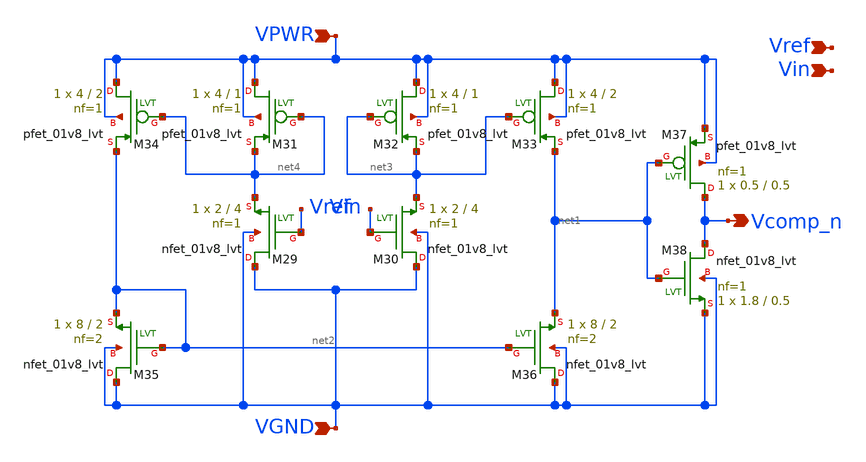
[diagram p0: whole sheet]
** sch_path: xschem/subckts/NComp.sch
**.subckt NComp Vcomp_n Vin Vref VPWR VGND
*.opin Vcomp_n
*.ipin Vin
*.ipin Vref
*.ipin VPWR
*.ipin VGND
XM29 VGND Vref net4 VGND sky130_fd_pr__nfet_01v8_lvt L=4 W=2 nf=1 ad='int((nf+1)/2) * W/nf * 0.29' as='int((nf+2)/2) * W/nf * 0.29'
+ pd='2*int((nf+1)/2) * (W/nf + 0.29)' ps='2*int((nf+2)/2) * (W/nf + 0.29)' nrd='0.29 / W' nrs='0.29 / W'
+ sa=0 sb=0 sd=0 mult=1 m=1
XM30 VGND Vin net3 VGND sky130_fd_pr__nfet_01v8_lvt L=4 W=2 nf=1 ad='int((nf+1)/2) * W/nf * 0.29' as='int((nf+2)/2) * W/nf * 0.29'
+ pd='2*int((nf+1)/2) * (W/nf + 0.29)' ps='2*int((nf+2)/2) * (W/nf + 0.29)' nrd='0.29 / W' nrs='0.29 / W'
+ sa=0 sb=0 sd=0 mult=1 m=1
XM31 VPWR net4 net4 VPWR sky130_fd_pr__pfet_01v8_lvt L=1 W=4 nf=1 ad='int((nf+1)/2) * W/nf * 0.29' as='int((nf+2)/2) * W/nf * 0.29'
+ pd='2*int((nf+1)/2) * (W/nf + 0.29)' ps='2*int((nf+2)/2) * (W/nf + 0.29)' nrd='0.29 / W' nrs='0.29 / W'
+ sa=0 sb=0 sd=0 mult=1 m=1
XM32 VPWR net3 net3 VPWR sky130_fd_pr__pfet_01v8_lvt L=1 W=4 nf=1 ad='int((nf+1)/2) * W/nf * 0.29' as='int((nf+2)/2) * W/nf * 0.29'
+ pd='2*int((nf+1)/2) * (W/nf + 0.29)' ps='2*int((nf+2)/2) * (W/nf + 0.29)' nrd='0.29 / W' nrs='0.29 / W'
+ sa=0 sb=0 sd=0 mult=1 m=1
XM33 VPWR net3 net1 VPWR sky130_fd_pr__pfet_01v8_lvt L=2 W=4 nf=1 ad='int((nf+1)/2) * W/nf * 0.29' as='int((nf+2)/2) * W/nf * 0.29'
+ pd='2*int((nf+1)/2) * (W/nf + 0.29)' ps='2*int((nf+2)/2) * (W/nf + 0.29)' nrd='0.29 / W' nrs='0.29 / W'
+ sa=0 sb=0 sd=0 mult=1 m=1
XM34 VPWR net4 net2 VPWR sky130_fd_pr__pfet_01v8_lvt L=2 W=4 nf=1 ad='int((nf+1)/2) * W/nf * 0.29' as='int((nf+2)/2) * W/nf * 0.29'
+ pd='2*int((nf+1)/2) * (W/nf + 0.29)' ps='2*int((nf+2)/2) * (W/nf + 0.29)' nrd='0.29 / W' nrs='0.29 / W'
+ sa=0 sb=0 sd=0 mult=1 m=1
XM35 VGND net2 net2 VGND sky130_fd_pr__nfet_01v8_lvt L=2 W=8 nf=2 ad='int((nf+1)/2) * W/nf * 0.29' as='int((nf+2)/2) * W/nf * 0.29'
+ pd='2*int((nf+1)/2) * (W/nf + 0.29)' ps='2*int((nf+2)/2) * (W/nf + 0.29)' nrd='0.29 / W' nrs='0.29 / W'
+ sa=0 sb=0 sd=0 mult=1 m=1
XM36 VGND net2 net1 VGND sky130_fd_pr__nfet_01v8_lvt L=2 W=8 nf=2 ad='int((nf+1)/2) * W/nf * 0.29' as='int((nf+2)/2) * W/nf * 0.29'
+ pd='2*int((nf+1)/2) * (W/nf + 0.29)' ps='2*int((nf+2)/2) * (W/nf + 0.29)' nrd='0.29 / W' nrs='0.29 / W'
+ sa=0 sb=0 sd=0 mult=1 m=1
XM37 Vcomp_n net1 VPWR VPWR sky130_fd_pr__pfet_01v8_lvt L=0.5 W=0.5 nf=1 ad='int((nf+1)/2) * W/nf * 0.29'
+ as='int((nf+2)/2) * W/nf * 0.29' pd='2*int((nf+1)/2) * (W/nf + 0.29)' ps='2*int((nf+2)/2) * (W/nf + 0.29)'
+ nrd='0.29 / W' nrs='0.29 / W' sa=0 sb=0 sd=0 mult=1 m=1
XM38 Vcomp_n net1 VGND VGND sky130_fd_pr__nfet_01v8_lvt L=0.5 W=1.8 nf=1 ad='int((nf+1)/2) * W/nf * 0.29'
+ as='int((nf+2)/2) * W/nf * 0.29' pd='2*int((nf+1)/2) * (W/nf + 0.29)' ps='2*int((nf+2)/2) * (W/nf + 0.29)'
+ nrd='0.29 / W' nrs='0.29 / W' sa=0 sb=0 sd=0 mult=1 m=1
**.ends
.end
